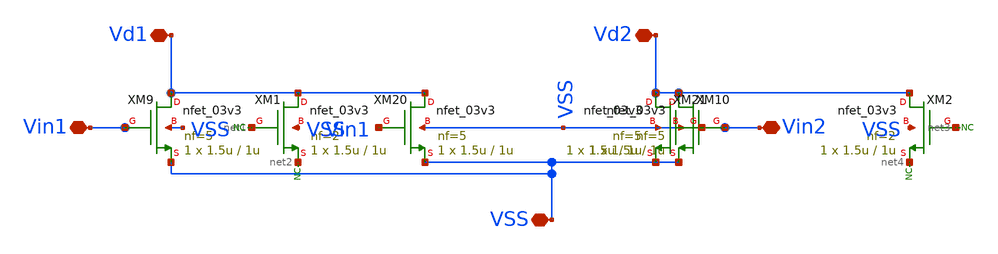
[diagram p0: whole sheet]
** sch_path: designs/comparator/final_magic/diffpairtest.sch
**.subckt diffpairtest Vin1 VSS Vd1 Vd2 Vin2
*.iopin Vin1
*.iopin VSS
*.iopin Vd1
*.iopin Vd2
*.iopin Vin2
XM9 Vd1 Vin1 VSS VSS nfet_03v3 L=1u W=1.5u nf=5 ad='int((nf+1)/2) * W/nf * 0.18u' as='int((nf+2)/2) * W/nf * 0.18u'
+ pd='2*int((nf+1)/2) * (W/nf + 0.18u)' ps='2*int((nf+2)/2) * (W/nf + 0.18u)' nrd='0.18u / W' nrs='0.18u / W'
+ sa=0 sb=0 sd=0 m=1
XM10 Vd2 Vin2 VSS VSS nfet_03v3 L=1u W=1.5u nf=5 ad='int((nf+1)/2) * W/nf * 0.18u' as='int((nf+2)/2) * W/nf * 0.18u'
+ pd='2*int((nf+1)/2) * (W/nf + 0.18u)' ps='2*int((nf+2)/2) * (W/nf + 0.18u)' nrd='0.18u / W' nrs='0.18u / W'
+ sa=0 sb=0 sd=0 m=1
XM20 Vd1 Vin1 VSS VSS nfet_03v3 L=1u W=1.5u nf=5 ad='int((nf+1)/2) * W/nf * 0.18u' as='int((nf+2)/2) * W/nf * 0.18u'
+ pd='2*int((nf+1)/2) * (W/nf + 0.18u)' ps='2*int((nf+2)/2) * (W/nf + 0.18u)' nrd='0.18u / W' nrs='0.18u / W'
+ sa=0 sb=0 sd=0 m=1
XM21 Vd2 Vin2 VSS VSS nfet_03v3 L=1u W=1.5u nf=5 ad='int((nf+1)/2) * W/nf * 0.18u' as='int((nf+2)/2) * W/nf * 0.18u'
+ pd='2*int((nf+1)/2) * (W/nf + 0.18u)' ps='2*int((nf+2)/2) * (W/nf + 0.18u)' nrd='0.18u / W' nrs='0.18u / W'
+ sa=0 sb=0 sd=0 m=1
XM1 Vd1 net1 net2 VSS nfet_03v3 L=1u W=1.5u nf=2 ad='int((nf+1)/2) * W/nf * 0.18u' as='int((nf+2)/2) * W/nf * 0.18u'
+ pd='2*int((nf+1)/2) * (W/nf + 0.18u)' ps='2*int((nf+2)/2) * (W/nf + 0.18u)' nrd='0.18u / W' nrs='0.18u / W'
+ sa=0 sb=0 sd=0 m=1
XM2 Vd2 net3 net4 VSS nfet_03v3 L=1u W=1.5u nf=2 ad='int((nf+1)/2) * W/nf * 0.18u' as='int((nf+2)/2) * W/nf * 0.18u'
+ pd='2*int((nf+1)/2) * (W/nf + 0.18u)' ps='2*int((nf+2)/2) * (W/nf + 0.18u)' nrd='0.18u / W' nrs='0.18u / W'
+ sa=0 sb=0 sd=0 m=1
* noconn #net3
* noconn #net4
* noconn #net2
* noconn #net1
**.ends
.end
